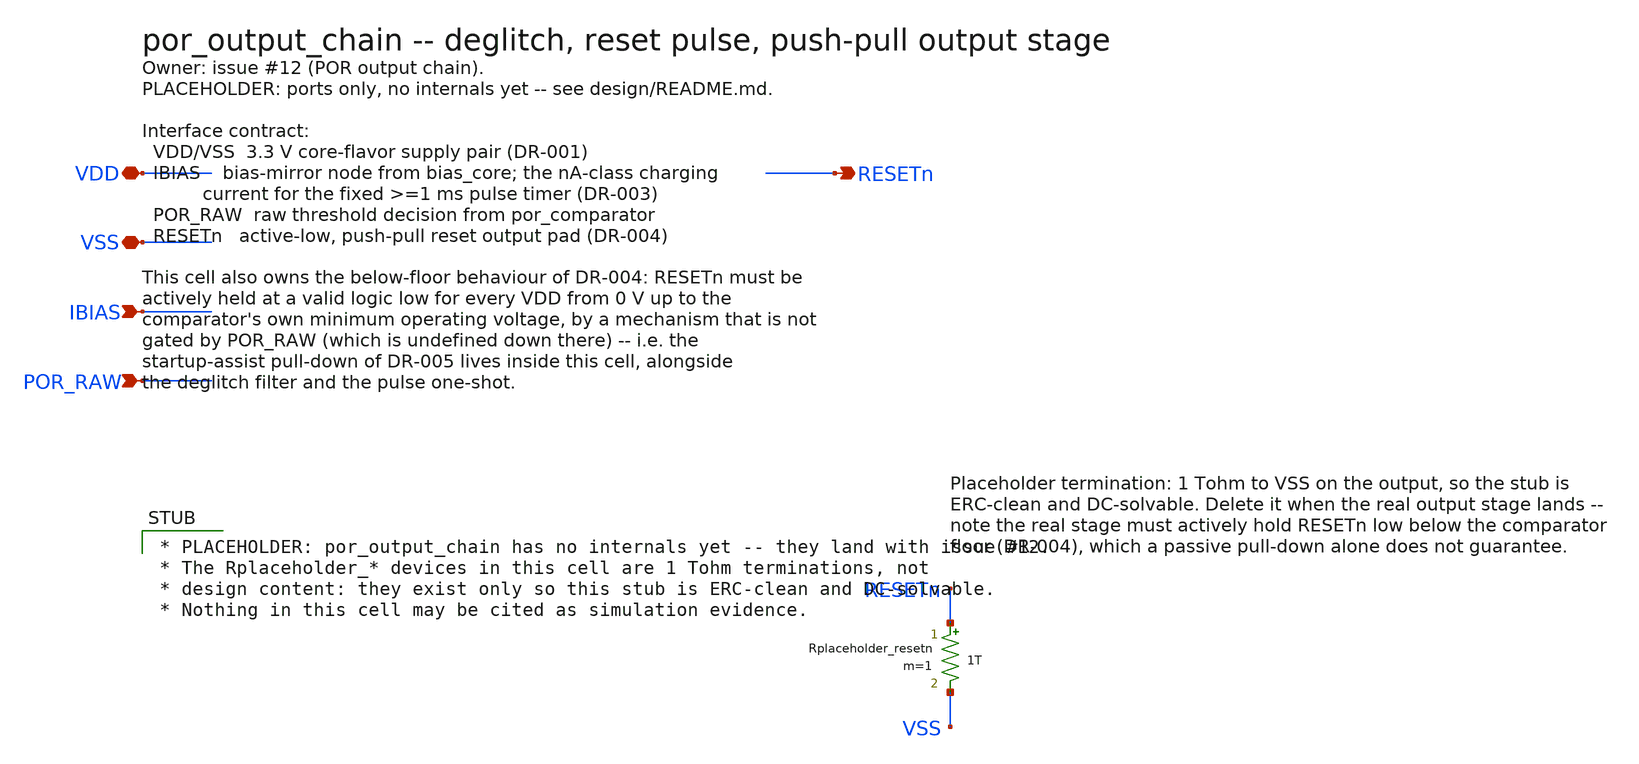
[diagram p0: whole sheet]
** sch_path: design/por_output_chain.sch
**.subckt por_output_chain VDD VSS IBIAS POR_RAW RESETn
*.iopin VDD
*.iopin VSS
*.ipin IBIAS
*.ipin POR_RAW
*.opin RESETn
Rplaceholder_resetn RESETn VSS 1T m=1
**** begin user architecture code

* PLACEHOLDER: por_output_chain has no internals yet -- they land with issue #12.
* The Rplaceholder_* devices in this cell are 1 Tohm terminations, not
* design content: they exist only so this stub is ERC-clean and DC-solvable.
* Nothing in this cell may be cited as simulation evidence.

**** end user architecture code
**.ends
.end
